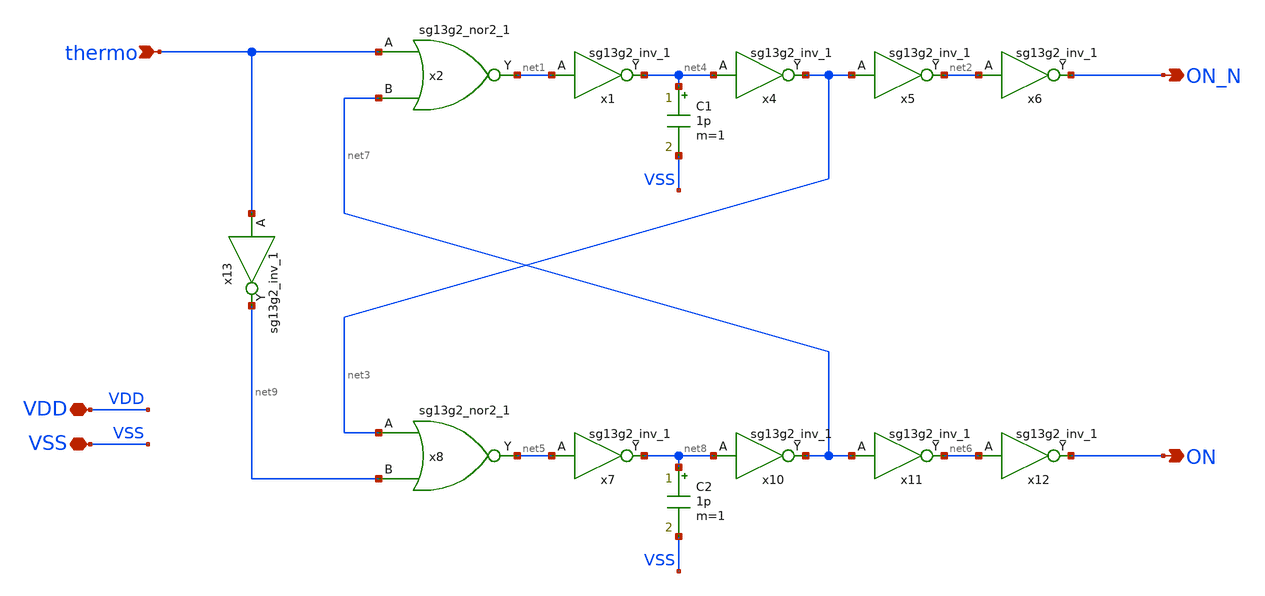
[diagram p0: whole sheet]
** sch_path: analog/non_overlap/xschem/non_overlap.sch
* IHP-GmbH/IHP-Open-PDK/ihp-sg13g2/libs.tech/xschem/sg13g2_stdcells/sg13g2_nor2_1.sch:
* Copyright 2023 IHP PDK Authors
* Licensed under the Apache License, Version 2.0 (the "License");
**.subckt non_overlap VSS thermo ON ON_N VDD
*.iopin VSS
*.ipin thermo
*.opin ON
*.opin ON_N
*.iopin VDD
x1 net4 net1 VDD VSS sg13g2_inv_1
x2 net1 thermo net7 VDD VSS sg13g2_nor2_1
x4 net3 net4 VDD VSS sg13g2_inv_1
x5 net2 net3 VDD VSS sg13g2_inv_1
x6 ON_N net2 VDD VSS sg13g2_inv_1
x7 net8 net5 VDD VSS sg13g2_inv_1
x8 net5 net3 net9 VDD VSS sg13g2_nor2_1
x10 net7 net8 VDD VSS sg13g2_inv_1
x11 net6 net7 VDD VSS sg13g2_inv_1
x12 ON net6 VDD VSS sg13g2_inv_1
x13 net9 thermo VDD VSS sg13g2_inv_1
C1 net4 VSS 1p m=1
C2 net8 VSS 1p m=1
**.ends

* expanding   symbol:  sg13g2_stdcells/sg13g2_inv_1.sym # of pins=2
** sym_path: sg13g2_stdcells/sg13g2_inv_1.sym
** sch_path: sg13g2_stdcells/sg13g2_inv_1.sch
.subckt sg13g2_inv_1 Y A VDD VSS
*.opin Y
*.ipin A
*.iopin VDD
*.iopin VSS
XM1 Y A VSS VSS sg13_lv_nmos w=740.00n l=130.00n ng=1 m=1 mm_ok=1
XM2 Y A VDD VDD sg13_lv_pmos w=1.12u l=130.00n ng=1 m=1 mm_ok=1
.ends


* expanding   symbol:  sg13g2_stdcells/sg13g2_nor2_1.sym # of pins=3
** sym_path: sg13g2_stdcells/sg13g2_nor2_1.sym
** sch_path: sg13g2_stdcells/sg13g2_nor2_1.sch
.subckt sg13g2_nor2_1 Y A B VDD VSS
*.opin Y
*.ipin B
*.ipin A
*.iopin VDD
*.iopin VSS
XM1 Y A VSS VSS sg13_lv_nmos w=740.00n l=130.00n ng=1 m=1 mm_ok=1
XM2 Y B VSS VSS sg13_lv_nmos w=740.00n l=130.00n ng=1 m=1 mm_ok=1
XM3 net1 A VDD VDD sg13_lv_pmos w=1.12u l=130.00n ng=1 m=1 mm_ok=1
XM4 Y B net1 VDD sg13_lv_pmos w=1.12u l=130.00n ng=1 m=1 mm_ok=1
.ends

.end
